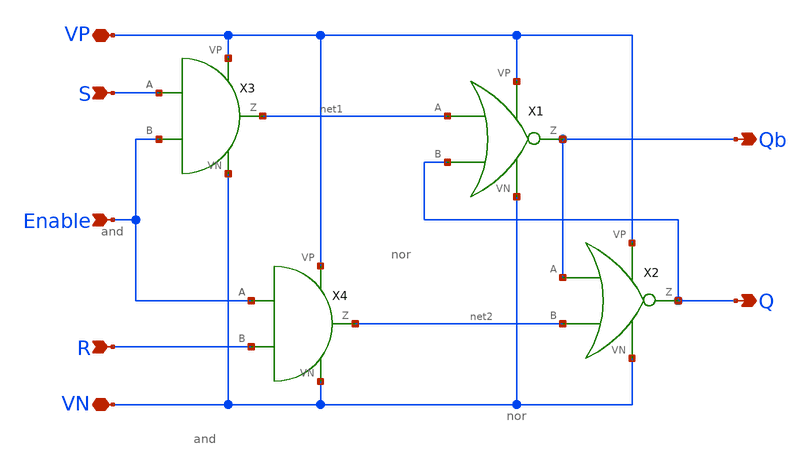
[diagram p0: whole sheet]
** sch_path: schematics/srlatch.sch
**.subckt srlatch S R VP VN Q Qb Enable
*.ipin S
*.ipin R
*.iopin VP
*.iopin VN
*.opin Q
*.opin Qb
*.ipin Enable
X1 net1 Q VP VN Qb nor
X2 Qb net2 VP VN Q nor
X3 S Enable VP VN net1 and
X4 Enable R VP VN net2 and
**.ends

* expanding   symbol:  /home/madvlsi/Documents/MADVLSI_final/schematics/nor.sym # of pins=5
** sym_path: schematics/nor.sym
** sch_path: schematics/nor.sch
.subckt nor A B VP VN Z
*.ipin A
*.ipin B
*.iopin VP
*.iopin VN
*.opin Z
**** begin user architecture code

.param l=.15
.param w=1

**** end user architecture code
XM1 Z A VN GND sky130_fd_pr__nfet_01v8 L=l W=w nf=1 ad='int((nf+1)/2) * W/nf * 0.29' as='int((nf+2)/2) * W/nf * 0.29'
+ pd='2*int((nf+1)/2) * (W/nf + 0.29)' ps='2*int((nf+2)/2) * (W/nf + 0.29)' nrd='0.29 / W' nrs='0.29 / W'
+ sa=0 sb=0 sd=0 mult=1 m=1
XM2 VN B Z GND sky130_fd_pr__nfet_01v8 L=l W=w nf=1 ad='int((nf+1)/2) * W/nf * 0.29' as='int((nf+2)/2) * W/nf * 0.29'
+ pd='2*int((nf+1)/2) * (W/nf + 0.29)' ps='2*int((nf+2)/2) * (W/nf + 0.29)' nrd='0.29 / W' nrs='0.29 / W'
+ sa=0 sb=0 sd=0 mult=1 m=1
XM3 Z A net1 VDD sky130_fd_pr__pfet_01v8 L=l W=w nf=1 ad='int((nf+1)/2) * W/nf * 0.29' as='int((nf+2)/2) * W/nf * 0.29'
+ pd='2*int((nf+1)/2) * (W/nf + 0.29)' ps='2*int((nf+2)/2) * (W/nf + 0.29)' nrd='0.29 / W' nrs='0.29 / W'
+ sa=0 sb=0 sd=0 mult=1 m=1
XM4 VP B net1 VDD sky130_fd_pr__pfet_01v8 L=l W=w nf=1 ad='int((nf+1)/2) * W/nf * 0.29' as='int((nf+2)/2) * W/nf * 0.29'
+ pd='2*int((nf+1)/2) * (W/nf + 0.29)' ps='2*int((nf+2)/2) * (W/nf + 0.29)' nrd='0.29 / W' nrs='0.29 / W'
+ sa=0 sb=0 sd=0 mult=1 m=1
.ends


* expanding   symbol:  /home/madvlsi/Documents/MADVLSI_final/schematics/and.sym # of pins=6
** sym_path: schematics/and.sym
** sch_path: schematics/and.sch
.subckt and A B VP VN Z
*.ipin A
*.ipin B
*.iopin VP
*.iopin VN
*.opin Z
X1 net1 VP VN Z inverter
X2 A B VP VN net1 nand
**** begin user architecture code

.param l=.15
.param w=1
.param mn=1
.param mp=1

**** end user architecture code
.ends


* expanding   symbol:  /home/madvlsi/Documents/final/xschem/inverter.sym # of pins=4
** sym_path: schematics/inverter.sym
** sch_path: schematics/inverter.sch
.subckt inverter A VP VN Z
*.ipin A
*.iopin VP
*.iopin VN
*.opin Z
XM1 Z A VN GND sky130_fd_pr__nfet_01v8 L=0.15 W=1 nf=1 ad='int((nf+1)/2) * W/nf * 0.29' as='int((nf+2)/2) * W/nf * 0.29'
+ pd='2*int((nf+1)/2) * (W/nf + 0.29)' ps='2*int((nf+2)/2) * (W/nf + 0.29)' nrd='0.29 / W' nrs='0.29 / W'
+ sa=0 sb=0 sd=0 mult=1 m=1
XM2 Z A VP VDD sky130_fd_pr__pfet_01v8 L=0.15 W=1 nf=1 ad='int((nf+1)/2) * W/nf * 0.29' as='int((nf+2)/2) * W/nf * 0.29'
+ pd='2*int((nf+1)/2) * (W/nf + 0.29)' ps='2*int((nf+2)/2) * (W/nf + 0.29)' nrd='0.29 / W' nrs='0.29 / W'
+ sa=0 sb=0 sd=0 mult=2 m=2
**** begin user architecture code

.param l=.15
.param w=1
.param mn=1
.param mp=1

**** end user architecture code
.ends


* expanding   symbol:  /home/madvlsi/Documents/final/xschem/nand.sym # of pins=6
** sym_path: schematics/nand.sym
** sch_path: schematics/nand.sch
.subckt nand A B VP VN Z
*.ipin A
*.iopin VP
*.iopin VN
*.opin Z
*.ipin B
XM1 Z A net1 GND sky130_fd_pr__nfet_01v8 L=0.15 W=1 nf=1 ad='int((nf+1)/2) * W/nf * 0.29' as='int((nf+2)/2) * W/nf * 0.29'
+ pd='2*int((nf+1)/2) * (W/nf + 0.29)' ps='2*int((nf+2)/2) * (W/nf + 0.29)' nrd='0.29 / W' nrs='0.29 / W'
+ sa=0 sb=0 sd=0 mult=1 m=1
XM2 VP B Z VDD sky130_fd_pr__pfet_01v8 L=0.15 W=1 nf=1 ad='int((nf+1)/2) * W/nf * 0.29' as='int((nf+2)/2) * W/nf * 0.29'
+ pd='2*int((nf+1)/2) * (W/nf + 0.29)' ps='2*int((nf+2)/2) * (W/nf + 0.29)' nrd='0.29 / W' nrs='0.29 / W'
+ sa=0 sb=0 sd=0 mult=2 m=2
XM3 VN B net1 GND sky130_fd_pr__nfet_01v8 L=0.15 W=1 nf=1 ad='int((nf+1)/2) * W/nf * 0.29' as='int((nf+2)/2) * W/nf * 0.29'
+ pd='2*int((nf+1)/2) * (W/nf + 0.29)' ps='2*int((nf+2)/2) * (W/nf + 0.29)' nrd='0.29 / W' nrs='0.29 / W'
+ sa=0 sb=0 sd=0 mult=1 m=1
XM4 Z A VP VDD sky130_fd_pr__pfet_01v8 L=0.15 W=1 nf=1 ad='int((nf+1)/2) * W/nf * 0.29' as='int((nf+2)/2) * W/nf * 0.29'
+ pd='2*int((nf+1)/2) * (W/nf + 0.29)' ps='2*int((nf+2)/2) * (W/nf + 0.29)' nrd='0.29 / W' nrs='0.29 / W'
+ sa=0 sb=0 sd=0 mult=2 m=2
.ends

.end
